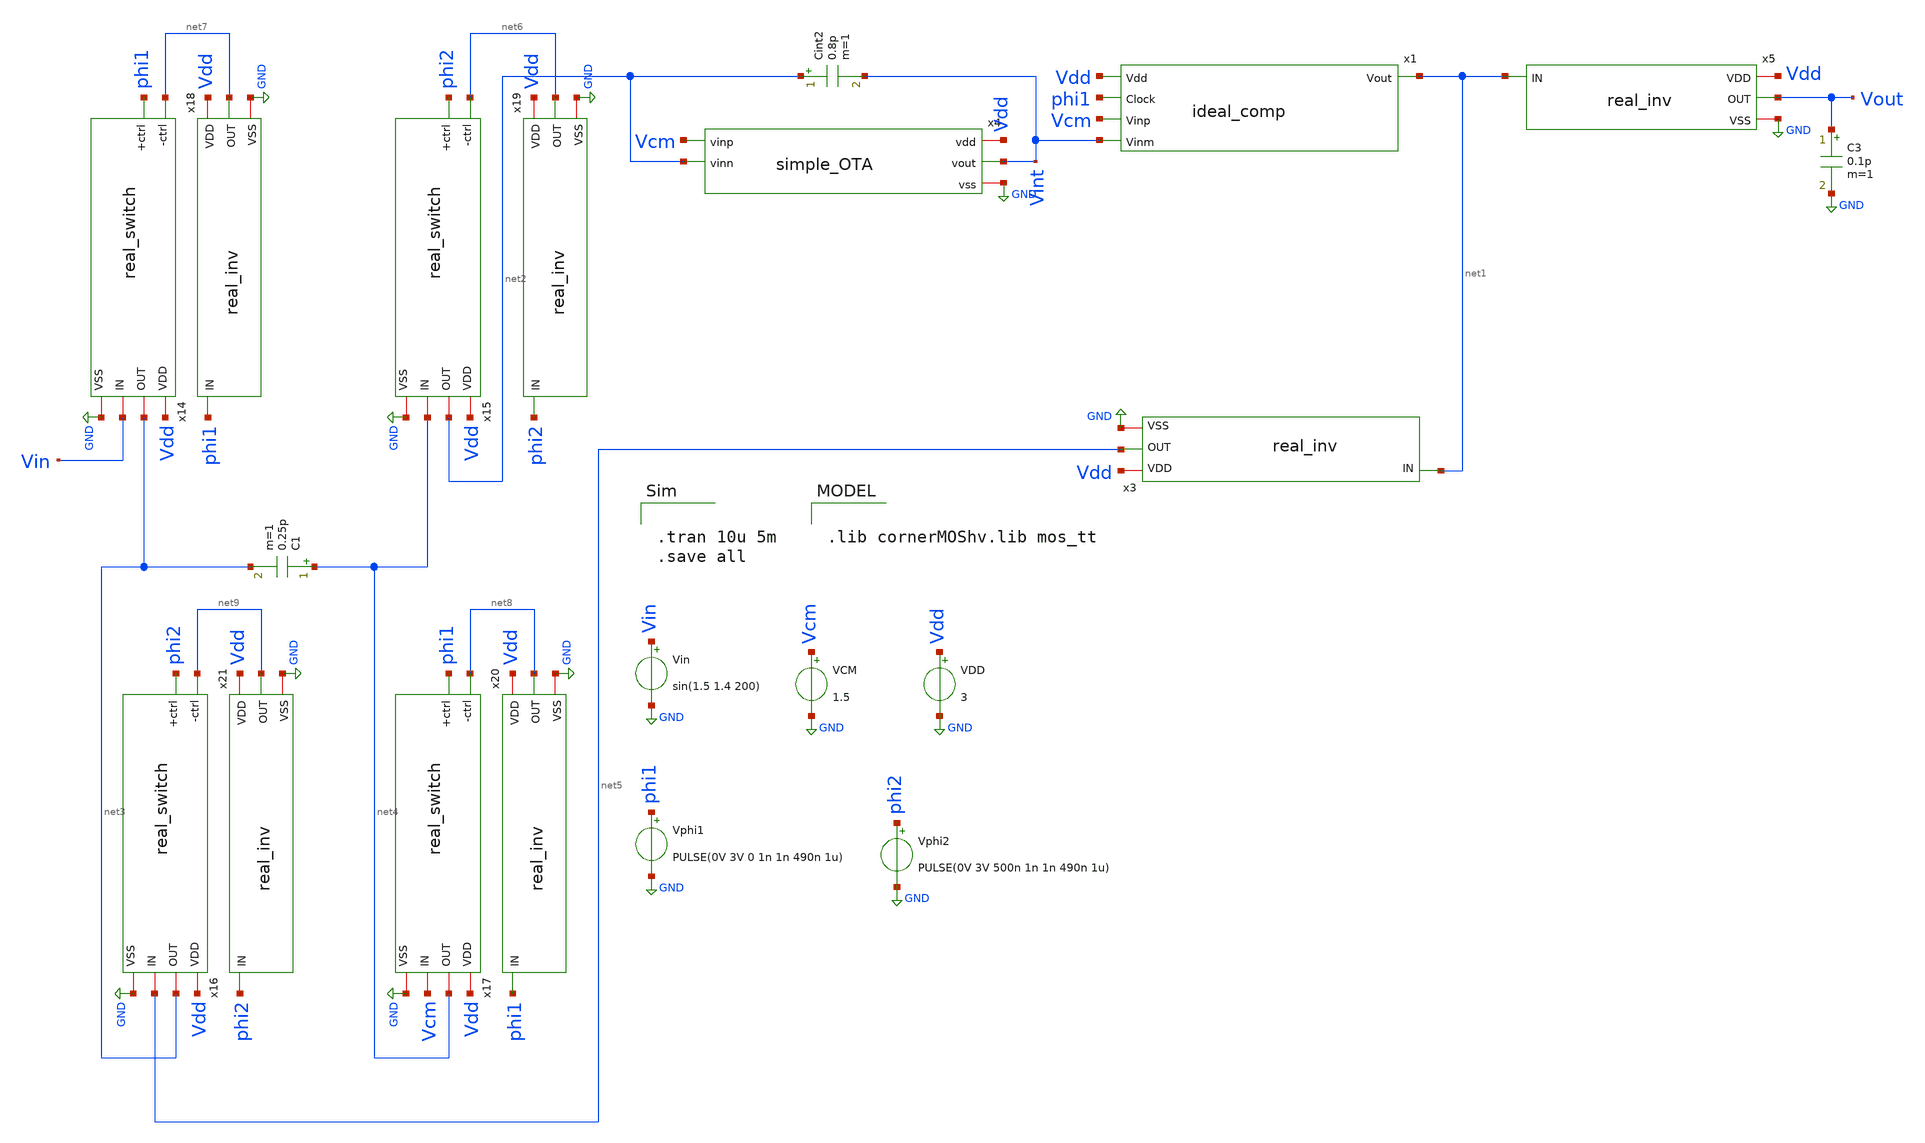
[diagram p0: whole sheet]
** sch_path: real_circuit/sandbox/first_order.sch
**.subckt first_order
Cint2 net2 Vint 0.8p m=1
x1 net1 Vdd phi1 Vcm Vint ideal_comp
VDD Vdd GND 3
VCM Vcm GND 1.5
Vin Vin GND sin(1.5 1.4 200)
Vphi1 phi1 GND PULSE(0V 3V 0 1n 1n 490n 1u)
Vphi2 phi2 GND PULSE(0V 3V 500n 1n 1n 490n 1u)
C1 net4 net3 0.25p m=1
x14 net7 Vdd net3 Vin phi1 GND real_switch
x15 net6 Vdd net2 net4 phi2 GND real_switch
x16 net9 Vdd net3 net5 phi2 GND real_switch
x17 net8 Vdd net4 Vcm phi1 GND real_switch
x18 Vdd phi1 net7 GND real_inv
x19 Vdd phi2 net6 GND real_inv
x20 Vdd phi1 net8 GND real_inv
x21 Vdd phi2 net9 GND real_inv
C3 Vout GND 0.1p m=1
x3 Vdd net1 net5 GND real_inv
x5 Vdd net1 Vout GND real_inv
x4 Vdd Vint Vcm net2 GND simple_OTA
**** begin user architecture code


.tran 10u 5m
.save all



.lib cornerMOShv.lib mos_tt

**** end user architecture code
**.ends
.GLOBAL GND
.end
